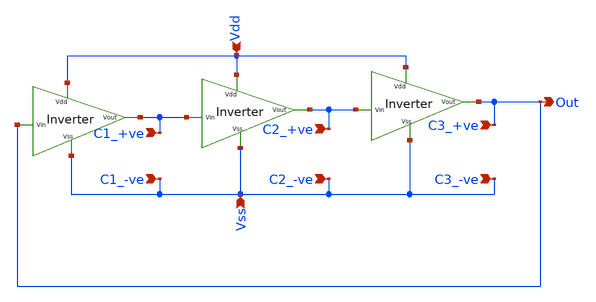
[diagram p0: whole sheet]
** sch_path: Xschem/Ring_Osc_3.sch
**.subckt Ring_Osc_3 Out Vss Vdd C1_-ve C1_+ve C2_-ve C2_+ve C3_+ve C3_-ve
*.opin Out
*.ipin Vss
*.ipin Vdd
*.ipin C1_-ve
*.ipin C1_+ve
*.ipin C2_-ve
*.ipin C2_+ve
*.ipin C3_+ve
*.ipin C3_-ve
x1 Vdd Out C1_+ve Vss inv
x2 Vdd C1_+ve C2_+ve Vss inv
x3 Vdd C2_+ve Out Vss inv
**.ends

* expanding   symbol:  inv.sym # of pins=4
** sym_path: Xschem/inv.sym
** sch_path: Xschem/inv.sch
.subckt inv Vdd Vin Vout Vss
*.ipin Vin
*.ipin Vss
*.ipin Vdd
*.opin Vout
XM1 Vout Vin Vss GND sky130_fd_pr__nfet_01v8 L=0.15 W=1 nf=1 ad='int((nf+1)/2) * W/nf * 0.29' as='int((nf+2)/2) * W/nf * 0.29'
+ pd='2*int((nf+1)/2) * (W/nf + 0.29)' ps='2*int((nf+2)/2) * (W/nf + 0.29)' nrd='0.29 / W' nrs='0.29 / W'
+ sa=0 sb=0 sd=0 mult=1 m=1
XM2 Vout Vin Vdd VDD sky130_fd_pr__pfet_01v8 L=0.15 W=2.5 nf=1 ad='int((nf+1)/2) * W/nf * 0.29' as='int((nf+2)/2) * W/nf * 0.29'
+ pd='2*int((nf+1)/2) * (W/nf + 0.29)' ps='2*int((nf+2)/2) * (W/nf + 0.29)' nrd='0.29 / W' nrs='0.29 / W'
+ sa=0 sb=0 sd=0 mult=1 m=1
.ends

.end
